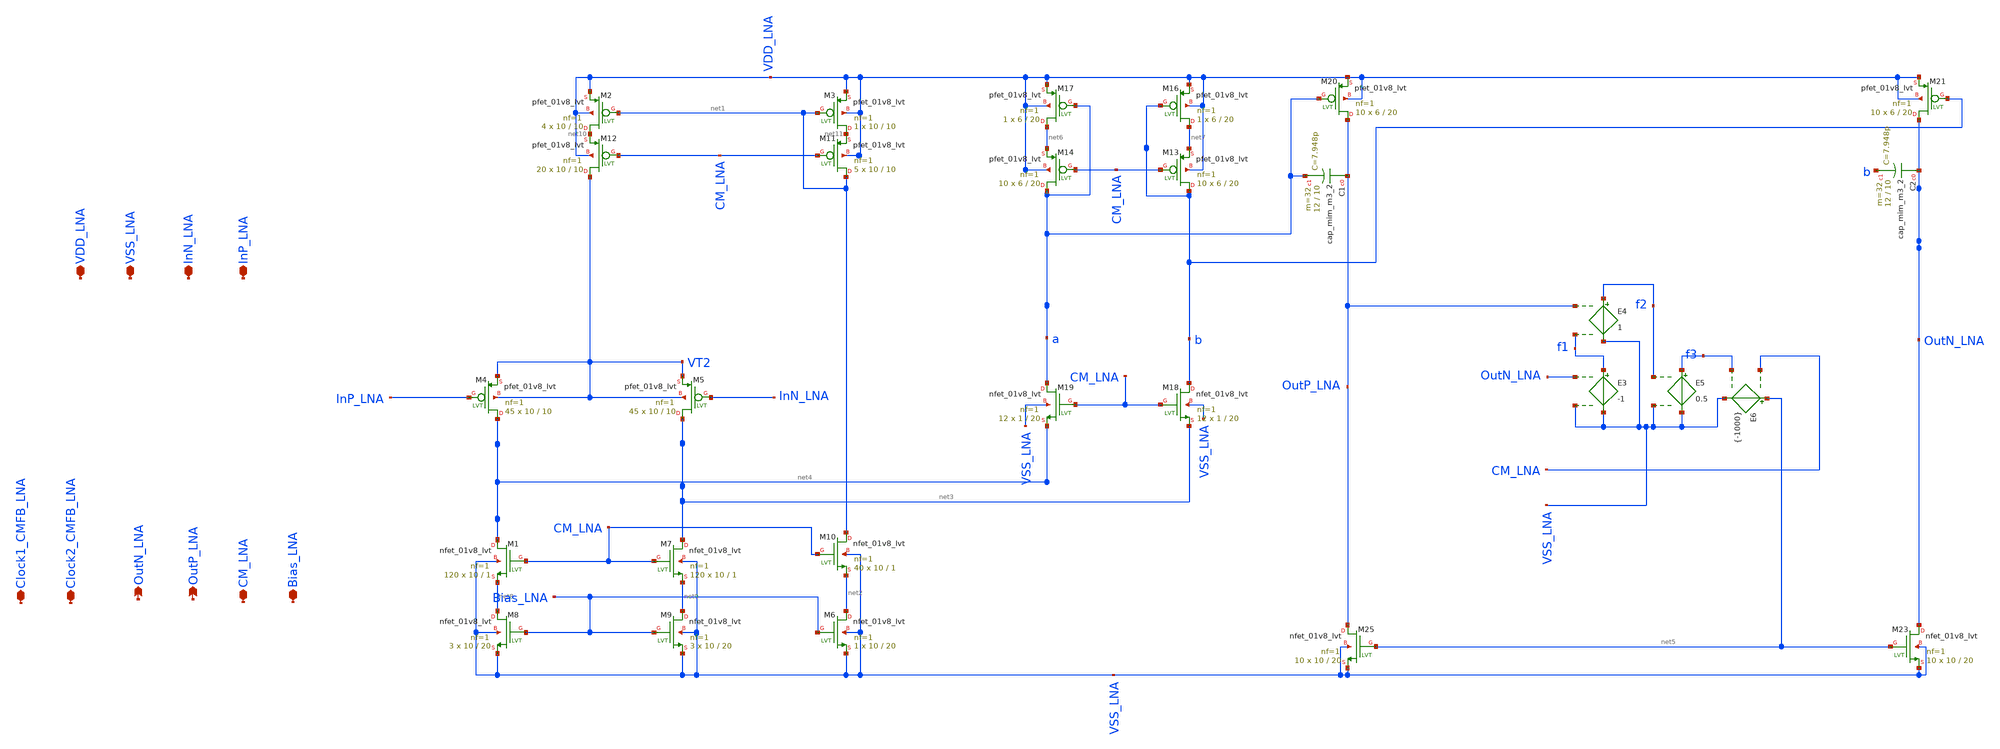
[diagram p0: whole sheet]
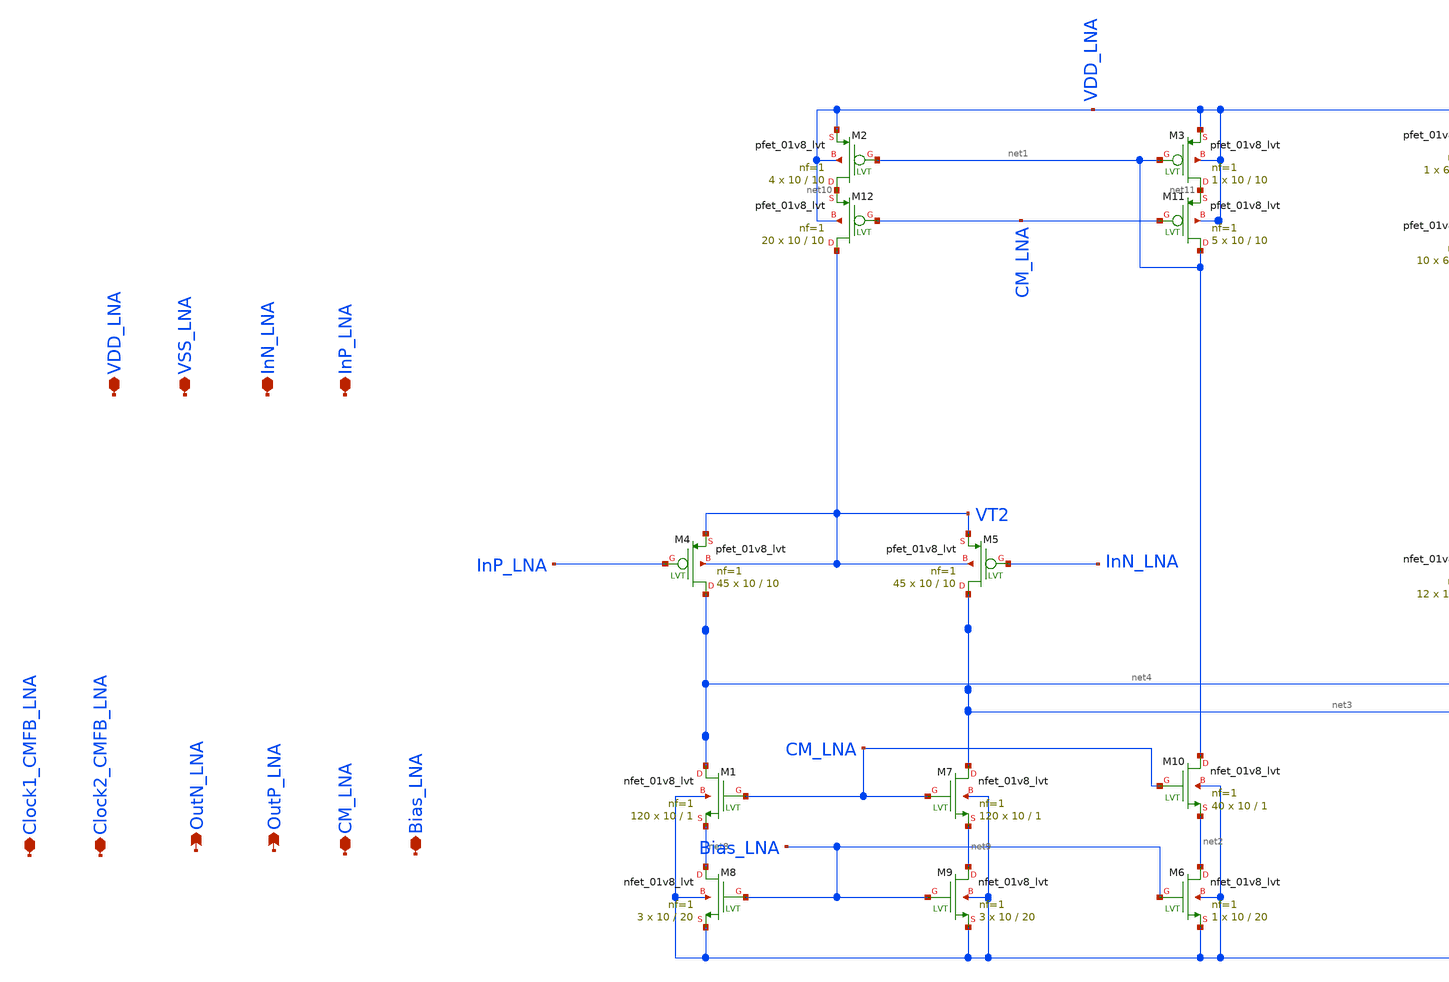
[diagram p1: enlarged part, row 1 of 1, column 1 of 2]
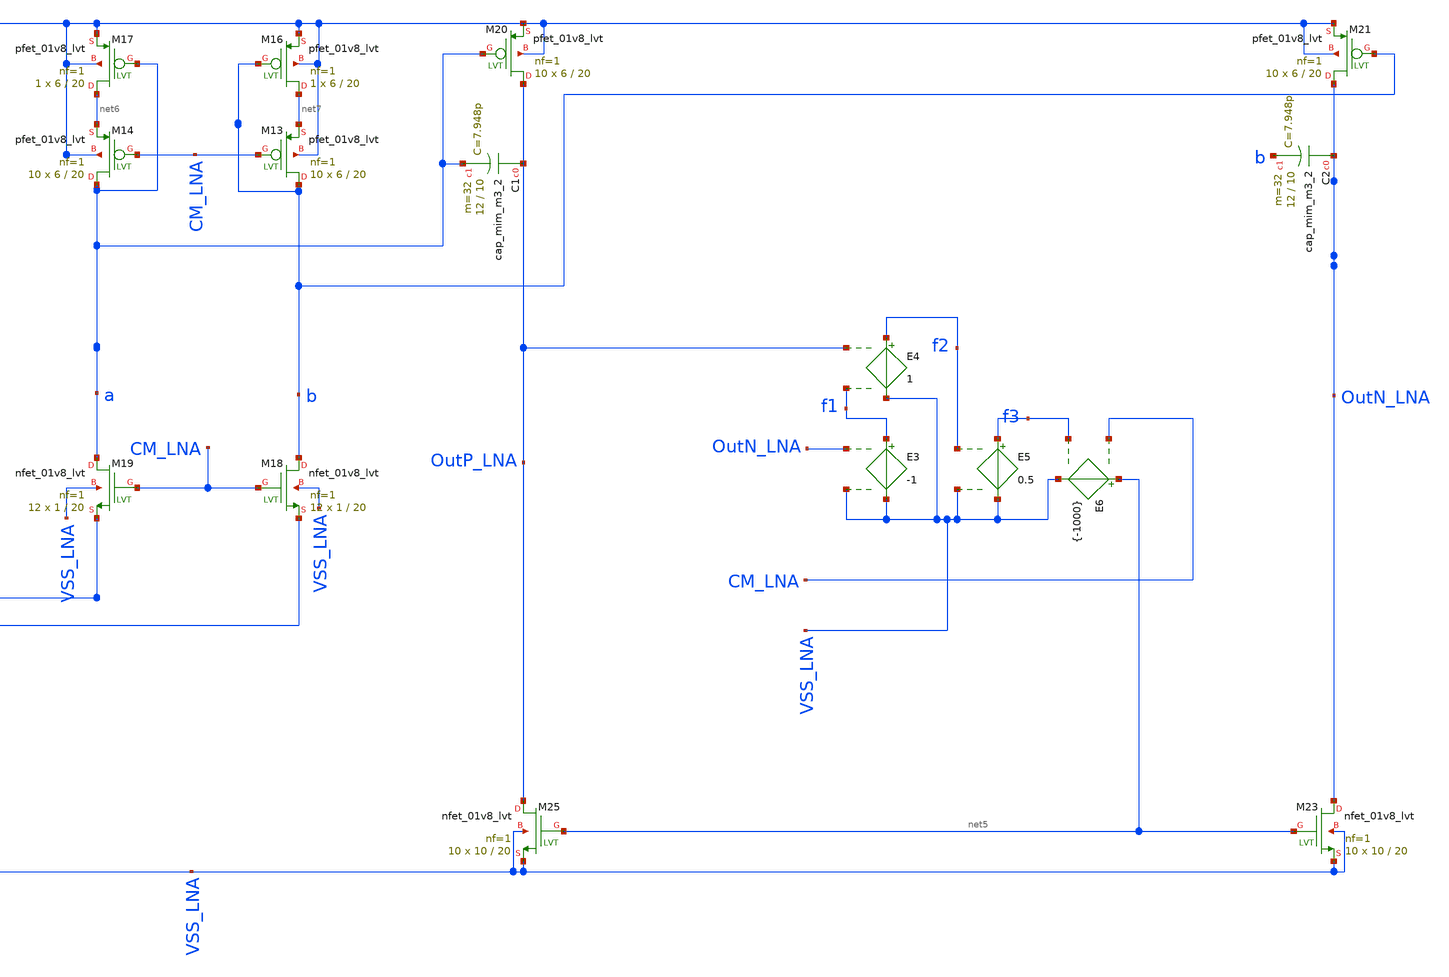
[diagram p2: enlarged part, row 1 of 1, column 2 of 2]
** sch_path: LNA_ac.sch
**.subckt LNA_ac InP_LNA InN_LNA VSS_LNA VDD_LNA CM_LNA OutP_LNA OutN_LNA Clock2_CMFB_LNA Bias_LNA
*+ Clock1_CMFB_LNA
*.iopin InP_LNA
*.iopin InN_LNA
*.iopin VSS_LNA
*.iopin VDD_LNA
*.iopin CM_LNA
*.opin OutP_LNA
*.opin OutN_LNA
*.iopin Clock2_CMFB_LNA
*.iopin Bias_LNA
*.iopin Clock1_CMFB_LNA
XM4 net4 InP_LNA VT2 VT2 sky130_fd_pr__pfet_01v8_lvt L=10 W=10 nf=1 ad='int((nf+1)/2) * W/nf * 0.29'
+ as='int((nf+2)/2) * W/nf * 0.29' pd='2*int((nf+1)/2) * (W/nf + 0.29)' ps='2*int((nf+2)/2) * (W/nf + 0.29)'
+ nrd='0.29 / W' nrs='0.29 / W' sa=0 sb=0 sd=0 mult=45 m=45
XM5 net3 InN_LNA VT2 VT2 sky130_fd_pr__pfet_01v8_lvt L=10 W=10 nf=1 ad='int((nf+1)/2) * W/nf * 0.29'
+ as='int((nf+2)/2) * W/nf * 0.29' pd='2*int((nf+1)/2) * (W/nf + 0.29)' ps='2*int((nf+2)/2) * (W/nf + 0.29)'
+ nrd='0.29 / W' nrs='0.29 / W' sa=0 sb=0 sd=0 mult=45 m=45
XM8 net8 Bias_LNA VSS_LNA VSS_LNA sky130_fd_pr__nfet_01v8_lvt L=20 W=10 nf=1 ad='int((nf+1)/2) * W/nf * 0.29'
+ as='int((nf+2)/2) * W/nf * 0.29' pd='2*int((nf+1)/2) * (W/nf + 0.29)' ps='2*int((nf+2)/2) * (W/nf + 0.29)'
+ nrd='0.29 / W' nrs='0.29 / W' sa=0 sb=0 sd=0 mult=3 m=3
XM9 net9 Bias_LNA VSS_LNA VSS_LNA sky130_fd_pr__nfet_01v8_lvt L=20 W=10 nf=1 ad='int((nf+1)/2) * W/nf * 0.29'
+ as='int((nf+2)/2) * W/nf * 0.29' pd='2*int((nf+1)/2) * (W/nf + 0.29)' ps='2*int((nf+2)/2) * (W/nf + 0.29)'
+ nrd='0.29 / W' nrs='0.29 / W' sa=0 sb=0 sd=0 mult=3 m=3
XM16 net7 b VDD_LNA VDD_LNA sky130_fd_pr__pfet_01v8_lvt L=20 W=6 nf=1 ad='int((nf+1)/2) * W/nf * 0.29'
+ as='int((nf+2)/2) * W/nf * 0.29' pd='2*int((nf+1)/2) * (W/nf + 0.29)' ps='2*int((nf+2)/2) * (W/nf + 0.29)'
+ nrd='0.29 / W' nrs='0.29 / W' sa=0 sb=0 sd=0 mult=1 m=1
XM17 net6 a VDD_LNA VDD_LNA sky130_fd_pr__pfet_01v8_lvt L=20 W=6 nf=1 ad='int((nf+1)/2) * W/nf * 0.29'
+ as='int((nf+2)/2) * W/nf * 0.29' pd='2*int((nf+1)/2) * (W/nf + 0.29)' ps='2*int((nf+2)/2) * (W/nf + 0.29)'
+ nrd='0.29 / W' nrs='0.29 / W' sa=0 sb=0 sd=0 mult=1 m=1
XM18 b CM_LNA net3 VSS_LNA sky130_fd_pr__nfet_01v8_lvt L=20 W=1 nf=1 ad='int((nf+1)/2) * W/nf * 0.29'
+ as='int((nf+2)/2) * W/nf * 0.29' pd='2*int((nf+1)/2) * (W/nf + 0.29)' ps='2*int((nf+2)/2) * (W/nf + 0.29)'
+ nrd='0.29 / W' nrs='0.29 / W' sa=0 sb=0 sd=0 mult=12 m=12
XM19 a CM_LNA net4 VSS_LNA sky130_fd_pr__nfet_01v8_lvt L=20 W=1 nf=1 ad='int((nf+1)/2) * W/nf * 0.29'
+ as='int((nf+2)/2) * W/nf * 0.29' pd='2*int((nf+1)/2) * (W/nf + 0.29)' ps='2*int((nf+2)/2) * (W/nf + 0.29)'
+ nrd='0.29 / W' nrs='0.29 / W' sa=0 sb=0 sd=0 mult=12 m=12
XM20 OutP_LNA a VDD_LNA VDD_LNA sky130_fd_pr__pfet_01v8_lvt L=20 W=6 nf=1 ad='int((nf+1)/2) * W/nf * 0.29'
+ as='int((nf+2)/2) * W/nf * 0.29' pd='2*int((nf+1)/2) * (W/nf + 0.29)' ps='2*int((nf+2)/2) * (W/nf + 0.29)'
+ nrd='0.29 / W' nrs='0.29 / W' sa=0 sb=0 sd=0 mult=10 m=10
XM21 OutN_LNA b VDD_LNA VDD_LNA sky130_fd_pr__pfet_01v8_lvt L=20 W=6 nf=1 ad='int((nf+1)/2) * W/nf * 0.29'
+ as='int((nf+2)/2) * W/nf * 0.29' pd='2*int((nf+1)/2) * (W/nf + 0.29)' ps='2*int((nf+2)/2) * (W/nf + 0.29)'
+ nrd='0.29 / W' nrs='0.29 / W' sa=0 sb=0 sd=0 mult=10 m=10
XM23 OutN_LNA net5 VSS_LNA VSS_LNA sky130_fd_pr__nfet_01v8_lvt L=20 W=10 nf=1 ad='int((nf+1)/2) * W/nf * 0.29'
+ as='int((nf+2)/2) * W/nf * 0.29' pd='2*int((nf+1)/2) * (W/nf + 0.29)' ps='2*int((nf+2)/2) * (W/nf + 0.29)'
+ nrd='0.29 / W' nrs='0.29 / W' sa=0 sb=0 sd=0 mult=10 m=10
XM25 OutP_LNA net5 VSS_LNA VSS_LNA sky130_fd_pr__nfet_01v8_lvt L=20 W=10 nf=1 ad='int((nf+1)/2) * W/nf * 0.29'
+ as='int((nf+2)/2) * W/nf * 0.29' pd='2*int((nf+1)/2) * (W/nf + 0.29)' ps='2*int((nf+2)/2) * (W/nf + 0.29)'
+ nrd='0.29 / W' nrs='0.29 / W' sa=0 sb=0 sd=0 mult=10 m=10
XM2 net10 net1 VDD_LNA VDD_LNA sky130_fd_pr__pfet_01v8_lvt L=10 W=10 nf=1 ad='int((nf+1)/2) * W/nf * 0.29'
+ as='int((nf+2)/2) * W/nf * 0.29' pd='2*int((nf+1)/2) * (W/nf + 0.29)' ps='2*int((nf+2)/2) * (W/nf + 0.29)'
+ nrd='0.29 / W' nrs='0.29 / W' sa=0 sb=0 sd=0 mult=4 m=4
XM3 net11 net1 VDD_LNA VDD_LNA sky130_fd_pr__pfet_01v8_lvt L=10 W=10 nf=1 ad='int((nf+1)/2) * W/nf * 0.29'
+ as='int((nf+2)/2) * W/nf * 0.29' pd='2*int((nf+1)/2) * (W/nf + 0.29)' ps='2*int((nf+2)/2) * (W/nf + 0.29)'
+ nrd='0.29 / W' nrs='0.29 / W' sa=0 sb=0 sd=0 mult=1 m=1
XM6 net2 Bias_LNA VSS_LNA VSS_LNA sky130_fd_pr__nfet_01v8_lvt L=20 W=10 nf=1 ad='int((nf+1)/2) * W/nf * 0.29'
+ as='int((nf+2)/2) * W/nf * 0.29' pd='2*int((nf+1)/2) * (W/nf + 0.29)' ps='2*int((nf+2)/2) * (W/nf + 0.29)'
+ nrd='0.29 / W' nrs='0.29 / W' sa=0 sb=0 sd=0 mult=1 m=1
E3 f1 VSS_LNA OutN_LNA VSS_LNA -1
E4 f2 VSS_LNA OutP_LNA f1 1
E5 f3 VSS_LNA f2 VSS_LNA 0.5
E6 net5 VSS_LNA CM_LNA f3 {-1000}
XC1 OutP_LNA a sky130_fd_pr__cap_mim_m3_2 W=12 L=10 MF=32 m=32
XC2 OutN_LNA b sky130_fd_pr__cap_mim_m3_2 W=12 L=10 MF=32 m=32
XM1 net4 CM_LNA net8 VSS_LNA sky130_fd_pr__nfet_01v8_lvt L=1 W=10 nf=1 ad='int((nf+1)/2) * W/nf * 0.29'
+ as='int((nf+2)/2) * W/nf * 0.29' pd='2*int((nf+1)/2) * (W/nf + 0.29)' ps='2*int((nf+2)/2) * (W/nf + 0.29)'
+ nrd='0.29 / W' nrs='0.29 / W' sa=0 sb=0 sd=0 mult=120 m=120
XM7 net3 CM_LNA net9 VSS_LNA sky130_fd_pr__nfet_01v8_lvt L=1 W=10 nf=1 ad='int((nf+1)/2) * W/nf * 0.29'
+ as='int((nf+2)/2) * W/nf * 0.29' pd='2*int((nf+1)/2) * (W/nf + 0.29)' ps='2*int((nf+2)/2) * (W/nf + 0.29)'
+ nrd='0.29 / W' nrs='0.29 / W' sa=0 sb=0 sd=0 mult=120 m=120
XM10 net1 CM_LNA net2 VSS_LNA sky130_fd_pr__nfet_01v8_lvt L=1 W=10 nf=1 ad='int((nf+1)/2) * W/nf * 0.29'
+ as='int((nf+2)/2) * W/nf * 0.29' pd='2*int((nf+1)/2) * (W/nf + 0.29)' ps='2*int((nf+2)/2) * (W/nf + 0.29)'
+ nrd='0.29 / W' nrs='0.29 / W' sa=0 sb=0 sd=0 mult=40 m=40
XM11 net1 CM_LNA net11 VDD_LNA sky130_fd_pr__pfet_01v8_lvt L=10 W=10 nf=1 ad='int((nf+1)/2) * W/nf * 0.29'
+ as='int((nf+2)/2) * W/nf * 0.29' pd='2*int((nf+1)/2) * (W/nf + 0.29)' ps='2*int((nf+2)/2) * (W/nf + 0.29)'
+ nrd='0.29 / W' nrs='0.29 / W' sa=0 sb=0 sd=0 mult=5 m=5
XM12 VT2 CM_LNA net10 VDD_LNA sky130_fd_pr__pfet_01v8_lvt L=10 W=10 nf=1 ad='int((nf+1)/2) * W/nf * 0.29'
+ as='int((nf+2)/2) * W/nf * 0.29' pd='2*int((nf+1)/2) * (W/nf + 0.29)' ps='2*int((nf+2)/2) * (W/nf + 0.29)'
+ nrd='0.29 / W' nrs='0.29 / W' sa=0 sb=0 sd=0 mult=20 m=20
XM13 b CM_LNA net7 VDD_LNA sky130_fd_pr__pfet_01v8_lvt L=20 W=6 nf=1 ad='int((nf+1)/2) * W/nf * 0.29'
+ as='int((nf+2)/2) * W/nf * 0.29' pd='2*int((nf+1)/2) * (W/nf + 0.29)' ps='2*int((nf+2)/2) * (W/nf + 0.29)'
+ nrd='0.29 / W' nrs='0.29 / W' sa=0 sb=0 sd=0 mult=10 m=10
XM14 a CM_LNA net6 VDD_LNA sky130_fd_pr__pfet_01v8_lvt L=20 W=6 nf=1 ad='int((nf+1)/2) * W/nf * 0.29'
+ as='int((nf+2)/2) * W/nf * 0.29' pd='2*int((nf+1)/2) * (W/nf + 0.29)' ps='2*int((nf+2)/2) * (W/nf + 0.29)'
+ nrd='0.29 / W' nrs='0.29 / W' sa=0 sb=0 sd=0 mult=10 m=10
**.ends
.end
